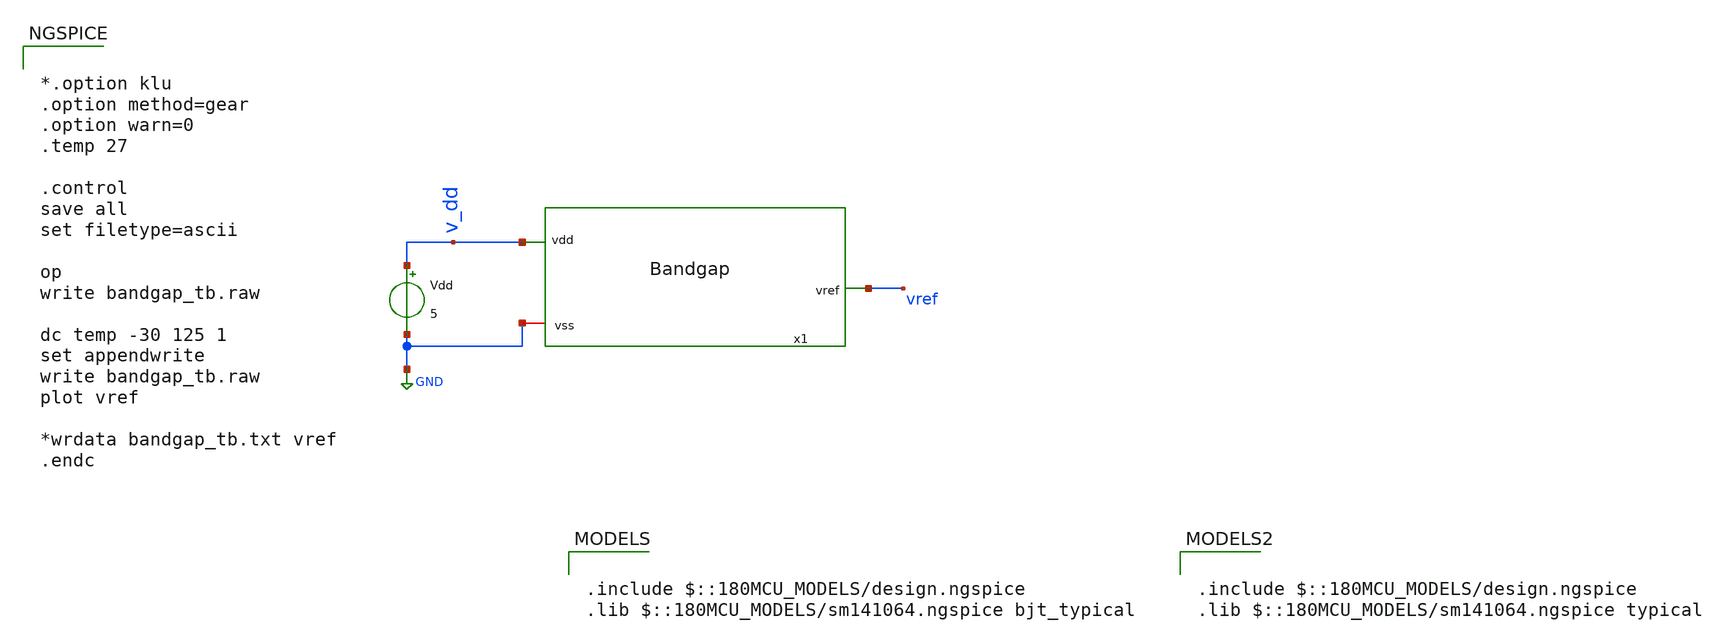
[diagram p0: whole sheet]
** sch_path: xschem/bandgap_tb.sch
**.subckt bandgap_tb
Vdd v_dd GND 5
x1 v_dd vref GND bandgap
**** begin user architecture code


*.option klu
.option method=gear
.option warn=0
.temp 27

.control
save all
set filetype=ascii

op
write bandgap_tb.raw

dc temp -30 125 1
set appendwrite
write bandgap_tb.raw
plot vref

*wrdata bandgap_tb.txt vref
.endc



.include $::180MCU_MODELS/design.ngspice
.lib $::180MCU_MODELS/sm141064.ngspice bjt_typical



.include $::180MCU_MODELS/design.ngspice
.lib $::180MCU_MODELS/sm141064.ngspice typical

**** end user architecture code
**.ends

* expanding   symbol:  bandgap.sym # of pins=3
** sym_path: xschem/bandgap.sym
** sch_path: xschem/bandgap.sch
.subckt bandgap vdd vref vss
*.ipin vdd
*.iopin vss
*.opin vref
XM1 net1 vg4 vdd vdd pfet_03v3 L=1u W=50u nf=10 ad='int((nf+1)/2) * W/nf * 0.18u' as='int((nf+2)/2) * W/nf * 0.18u'
+ pd='2*int((nf+1)/2) * (W/nf + 0.18u)' ps='2*int((nf+2)/2) * (W/nf + 0.18u)' nrd='0.18u / W' nrs='0.18u / W'
+ sa=0 sb=0 sd=0 m=1
XM2 vg2 vg3 net1 vdd pfet_03v3 L=1u W=50u nf=10 ad='int((nf+1)/2) * W/nf * 0.18u' as='int((nf+2)/2) * W/nf * 0.18u'
+ pd='2*int((nf+1)/2) * (W/nf + 0.18u)' ps='2*int((nf+2)/2) * (W/nf + 0.18u)' nrd='0.18u / W' nrs='0.18u / W'
+ sa=0 sb=0 sd=0 m=1
XM3 net2 vg4 vdd vdd pfet_03v3 L=1u W=50u nf=10 ad='int((nf+1)/2) * W/nf * 0.18u' as='int((nf+2)/2) * W/nf * 0.18u'
+ pd='2*int((nf+1)/2) * (W/nf + 0.18u)' ps='2*int((nf+2)/2) * (W/nf + 0.18u)' nrd='0.18u / W' nrs='0.18u / W'
+ sa=0 sb=0 sd=0 m=1
XM4 vg4 vg3 net2 vdd pfet_03v3 L=1u W=50u nf=10 ad='int((nf+1)/2) * W/nf * 0.18u' as='int((nf+2)/2) * W/nf * 0.18u'
+ pd='2*int((nf+1)/2) * (W/nf + 0.18u)' ps='2*int((nf+2)/2) * (W/nf + 0.18u)' nrd='0.18u / W' nrs='0.18u / W'
+ sa=0 sb=0 sd=0 m=1
R1 vg4 vg3 10.16k m=1
XM5 net3 vg4 vdd vdd pfet_03v3 L=1u W=50u nf=10 ad='int((nf+1)/2) * W/nf * 0.18u' as='int((nf+2)/2) * W/nf * 0.18u'
+ pd='2*int((nf+1)/2) * (W/nf + 0.18u)' ps='2*int((nf+2)/2) * (W/nf + 0.18u)' nrd='0.18u / W' nrs='0.18u / W'
+ sa=0 sb=0 sd=0 m=1
XM6 vref vg3 net3 vdd pfet_03v3 L=1u W=50u nf=10 ad='int((nf+1)/2) * W/nf * 0.18u' as='int((nf+2)/2) * W/nf * 0.18u'
+ pd='2*int((nf+1)/2) * (W/nf + 0.18u)' ps='2*int((nf+2)/2) * (W/nf + 0.18u)' nrd='0.18u / W' nrs='0.18u / W'
+ sa=0 sb=0 sd=0 m=1
R2 vref net4 37.5k m=1
XQ1 vss vss net4 pnp_05p00x05p00 m=40 par=40
XM7 vg3 vg2 net5 vss nfet_03v3 L=1u W=15u nf=3 ad='int((nf+1)/2) * W/nf * 0.18u' as='int((nf+2)/2) * W/nf * 0.18u'
+ pd='2*int((nf+1)/2) * (W/nf + 0.18u)' ps='2*int((nf+2)/2) * (W/nf + 0.18u)' nrd='0.18u / W' nrs='0.18u / W'
+ sa=0 sb=0 sd=0 m=1
XM8 net5 vg1 net7 vss nfet_03v3 L=1u W=15u nf=3 ad='int((nf+1)/2) * W/nf * 0.18u' as='int((nf+2)/2) * W/nf * 0.18u'
+ pd='2*int((nf+1)/2) * (W/nf + 0.18u)' ps='2*int((nf+2)/2) * (W/nf + 0.18u)' nrd='0.18u / W' nrs='0.18u / W'
+ sa=0 sb=0 sd=0 m=1
R3 net7 net6 6.306k m=1
XQ2 vss vss net6 pnp_05p00x05p00 m=40 par=40
XM9 vg1 vg2 net8 vss nfet_03v3 L=1u W=15u nf=3 ad='int((nf+1)/2) * W/nf * 0.18u' as='int((nf+2)/2) * W/nf * 0.18u'
+ pd='2*int((nf+1)/2) * (W/nf + 0.18u)' ps='2*int((nf+2)/2) * (W/nf + 0.18u)' nrd='0.18u / W' nrs='0.18u / W'
+ sa=0 sb=0 sd=0 m=1
R4 vg2 vg1 10.16k m=1
XM10 net8 vg1 net9 vss nfet_03v3 L=1u W=15u nf=3 ad='int((nf+1)/2) * W/nf * 0.18u' as='int((nf+2)/2) * W/nf * 0.18u'
+ pd='2*int((nf+1)/2) * (W/nf + 0.18u)' ps='2*int((nf+2)/2) * (W/nf + 0.18u)' nrd='0.18u / W' nrs='0.18u / W'
+ sa=0 sb=0 sd=0 m=1
XM11 vg2 vg2 vg3 vdd pfet_03v3 L=10u W=0.5u nf=1 ad='int((nf+1)/2) * W/nf * 0.18u' as='int((nf+2)/2) * W/nf * 0.18u'
+ pd='2*int((nf+1)/2) * (W/nf + 0.18u)' ps='2*int((nf+2)/2) * (W/nf + 0.18u)' nrd='0.18u / W' nrs='0.18u / W'
+ sa=0 sb=0 sd=0 m=1
XQ3 vss vss net9 pnp_05p00x05p00 m=2 par=2
.ends

.GLOBAL GND
.end
